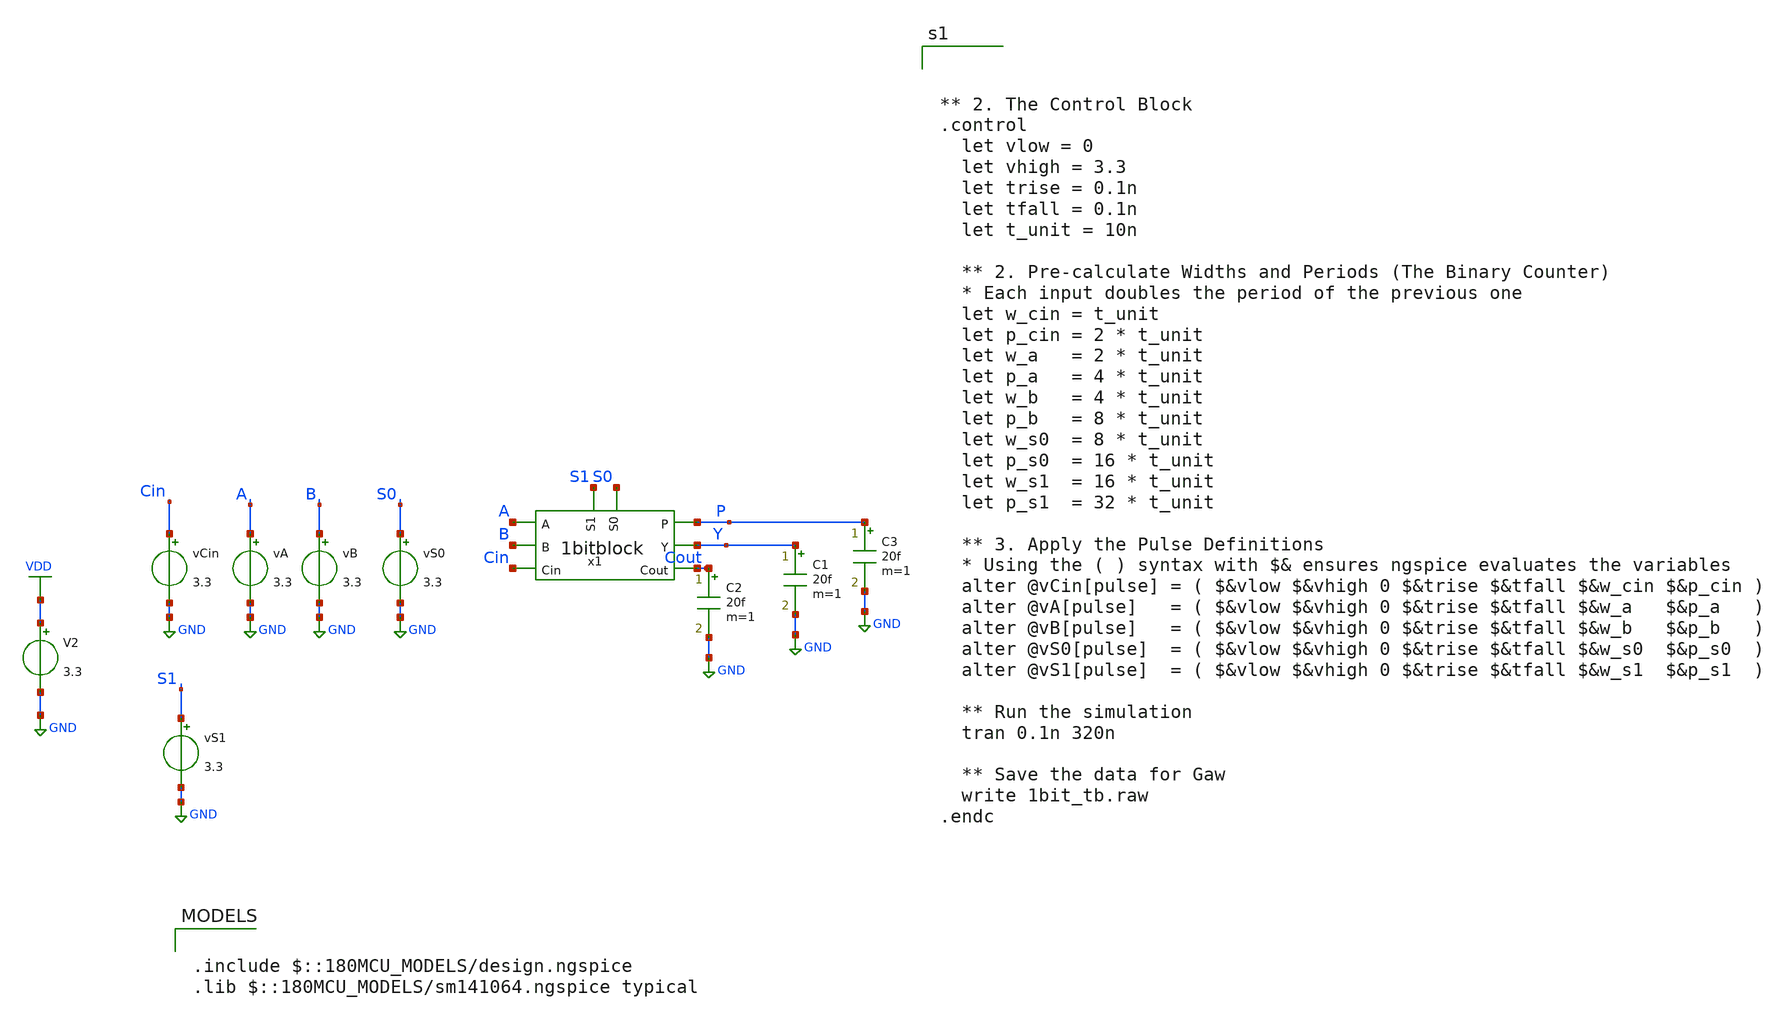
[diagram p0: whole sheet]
** sch_path: tbs/1bit_tb.sch
**.subckt 1bit_tb
vA A GND 3.3
vCin Cin GND 3.3
vS0 S0 GND 3.3
vB B GND 3.3
vS1 S1 GND 3.3
C2 Cout GND 20f m=1
C1 Y GND 20f m=1
C3 P GND 20f m=1
x1 P A B Cin S0 S1 Y Cout 1bitblock
V2 VDD GND 3.3
**** begin user architecture code

.include $::180MCU_MODELS/design.ngspice
.lib $::180MCU_MODELS/sm141064.ngspice typical




** 2. The Control Block
.control
  let vlow = 0
  let vhigh = 3.3
  let trise = 0.1n
  let tfall = 0.1n
  let t_unit = 10n

  ** 2. Pre-calculate Widths and Periods (The Binary Counter)
  * Each input doubles the period of the previous one
  let w_cin = t_unit
  let p_cin = 2 * t_unit
  let w_a   = 2 * t_unit
  let p_a   = 4 * t_unit
  let w_b   = 4 * t_unit
  let p_b   = 8 * t_unit
  let w_s0  = 8 * t_unit
  let p_s0  = 16 * t_unit
  let w_s1  = 16 * t_unit
  let p_s1  = 32 * t_unit

  ** 3. Apply the Pulse Definitions
  * Using the ( ) syntax with $& ensures ngspice evaluates the variables
  alter @vCin[pulse] = ( $&vlow $&vhigh 0 $&trise $&tfall $&w_cin $&p_cin )
  alter @vA[pulse]   = ( $&vlow $&vhigh 0 $&trise $&tfall $&w_a   $&p_a   )
  alter @vB[pulse]   = ( $&vlow $&vhigh 0 $&trise $&tfall $&w_b   $&p_b   )
  alter @vS0[pulse]  = ( $&vlow $&vhigh 0 $&trise $&tfall $&w_s0  $&p_s0  )
  alter @vS1[pulse]  = ( $&vlow $&vhigh 0 $&trise $&tfall $&w_s1  $&p_s1  )

  ** Run the simulation
  tran 0.1n 320n

  ** Save the data for Gaw
  write 1bit_tb.raw
.endc


**** end user architecture code
**.ends
.GLOBAL GND
.GLOBAL VDD
.end
